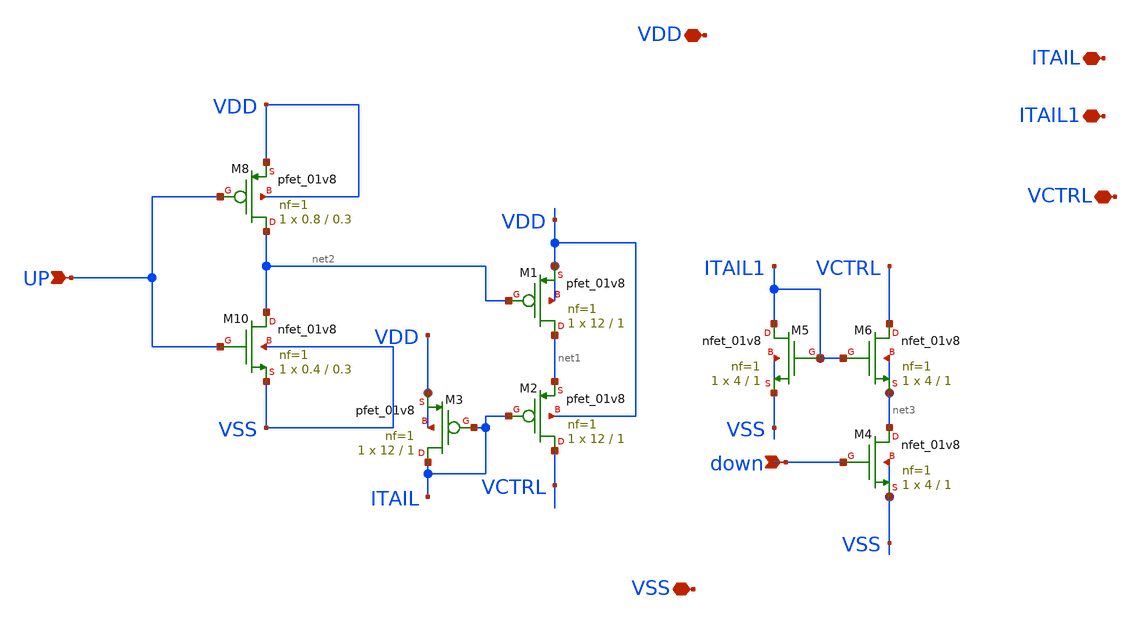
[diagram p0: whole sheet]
** sch_path: Xschem/PLL_TOP_Schematics/CP.sch
**.subckt CP UP down VCTRL VDD VSS ITAIL1 ITAIL
*.ipin UP
*.ipin down
*.iopin VCTRL
*.iopin VDD
*.iopin VSS
*.iopin ITAIL1
*.iopin ITAIL
XM8 net2 UP VDD VDD sky130_fd_pr__pfet_01v8 L=0.3 W=0.8 nf=1 ad='int((nf+1)/2) * W/nf * 0.29' as='int((nf+2)/2) * W/nf * 0.29'
+ pd='2*int((nf+1)/2) * (W/nf + 0.29)' ps='2*int((nf+2)/2) * (W/nf + 0.29)' nrd='0.29 / W' nrs='0.29 / W'
+ sa=0 sb=0 sd=0 mult=1 m=1
XM1 net1 net2 VDD VDD sky130_fd_pr__pfet_01v8 L=1 W=12 nf=1 ad='int((nf+1)/2) * W/nf * 0.29' as='int((nf+2)/2) * W/nf * 0.29'
+ pd='2*int((nf+1)/2) * (W/nf + 0.29)' ps='2*int((nf+2)/2) * (W/nf + 0.29)' nrd='0.29 / W' nrs='0.29 / W'
+ sa=0 sb=0 sd=0 mult=1 m=1
XM10 net2 UP VSS VSS sky130_fd_pr__nfet_01v8 L=0.3 W=0.4 nf=1 ad='int((nf+1)/2) * W/nf * 0.29' as='int((nf+2)/2) * W/nf * 0.29'
+ pd='2*int((nf+1)/2) * (W/nf + 0.29)' ps='2*int((nf+2)/2) * (W/nf + 0.29)' nrd='0.29 / W' nrs='0.29 / W'
+ sa=0 sb=0 sd=0 mult=1 m=1
XM2 VCTRL ITAIL net1 VDD sky130_fd_pr__pfet_01v8 L=1 W=12 nf=1 ad='int((nf+1)/2) * W/nf * 0.29' as='int((nf+2)/2) * W/nf * 0.29'
+ pd='2*int((nf+1)/2) * (W/nf + 0.29)' ps='2*int((nf+2)/2) * (W/nf + 0.29)' nrd='0.29 / W' nrs='0.29 / W'
+ sa=0 sb=0 sd=0 mult=1 m=1
XM3 ITAIL ITAIL VDD VDD sky130_fd_pr__pfet_01v8 L=1 W=12 nf=1 ad='int((nf+1)/2) * W/nf * 0.29' as='int((nf+2)/2) * W/nf * 0.29'
+ pd='2*int((nf+1)/2) * (W/nf + 0.29)' ps='2*int((nf+2)/2) * (W/nf + 0.29)' nrd='0.29 / W' nrs='0.29 / W'
+ sa=0 sb=0 sd=0 mult=1 m=1
XM5 ITAIL1 ITAIL1 VSS VSS sky130_fd_pr__nfet_01v8 L=1 W=4 nf=1 ad='int((nf+1)/2) * W/nf * 0.29' as='int((nf+2)/2) * W/nf * 0.29'
+ pd='2*int((nf+1)/2) * (W/nf + 0.29)' ps='2*int((nf+2)/2) * (W/nf + 0.29)' nrd='0.29 / W' nrs='0.29 / W'
+ sa=0 sb=0 sd=0 mult=1 m=1
XM6 VCTRL ITAIL1 net3 net3 sky130_fd_pr__nfet_01v8 L=1 W=4 nf=1 ad='int((nf+1)/2) * W/nf * 0.29' as='int((nf+2)/2) * W/nf * 0.29'
+ pd='2*int((nf+1)/2) * (W/nf + 0.29)' ps='2*int((nf+2)/2) * (W/nf + 0.29)' nrd='0.29 / W' nrs='0.29 / W'
+ sa=0 sb=0 sd=0 mult=1 m=1
XM4 net3 down VSS VSS sky130_fd_pr__nfet_01v8 L=1 W=4 nf=1 ad='int((nf+1)/2) * W/nf * 0.29' as='int((nf+2)/2) * W/nf * 0.29'
+ pd='2*int((nf+1)/2) * (W/nf + 0.29)' ps='2*int((nf+2)/2) * (W/nf + 0.29)' nrd='0.29 / W' nrs='0.29 / W'
+ sa=0 sb=0 sd=0 mult=1 m=1
**.ends
.end
